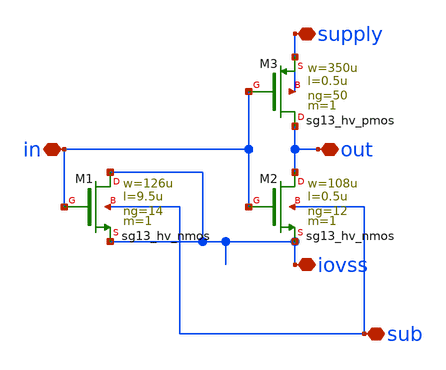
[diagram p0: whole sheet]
** sch_path: MSPHY6034-main/dependencies/unic_cass_2025_team04_padring/xschem/openpdk-libraries/ihp-sg13g2/sg13g2_io/xschem/sg13g2_RCClampInverter_noptap.sch
**.subckt sg13g2_RCClampInverter_noptap supply iovss out in sub
*.iopin supply
*.iopin iovss
*.iopin out
*.iopin in
*.iopin sub
XM1 iovss in iovss sub sg13_hv_nmos w=126u l=9.5u ng=14 m=1 mm_ok=1
XM2 out in iovss sub sg13_hv_nmos w=108u l=0.5u ng=12 m=1 mm_ok=1
XM3 out in supply supply sg13_hv_pmos w=350u l=0.5u ng=50 m=1 mm_ok=1
**.ends
.end
